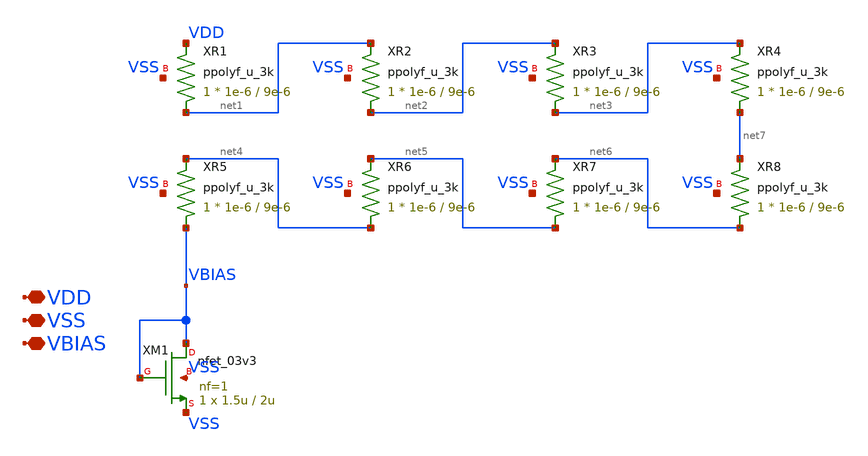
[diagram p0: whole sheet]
** sch_path: designs/libs/core_current-mirror/nbias-gen/nbias-gen.sch
**.subckt nbias-gen VDD VSS VBIAS
*.iopin VDD
*.iopin VSS
*.iopin VBIAS
XM1 VBIAS VBIAS VSS VSS nfet_03v3 L=2u W=1.5u nf=1 ad='int((nf+1)/2) * W/nf * 0.18u' as='int((nf+2)/2) * W/nf * 0.18u'
+ pd='2*int((nf+1)/2) * (W/nf + 0.18u)' ps='2*int((nf+2)/2) * (W/nf + 0.18u)' nrd='0.18u / W' nrs='0.18u / W'
+ sa=0 sb=0 sd=0 m=1
XR1 net1 VDD VSS ppolyf_u_3k r_width=1e-6 r_length=9e-6 m=1
XR2 net2 net1 VSS ppolyf_u_3k r_width=1e-6 r_length=9e-6 m=1
XR3 net3 net2 VSS ppolyf_u_3k r_width=1e-6 r_length=9e-6 m=1
XR4 net7 net3 VSS ppolyf_u_3k r_width=1e-6 r_length=9e-6 m=1
XR5 VBIAS net4 VSS ppolyf_u_3k r_width=1e-6 r_length=9e-6 m=1
XR6 net4 net5 VSS ppolyf_u_3k r_width=1e-6 r_length=9e-6 m=1
XR7 net5 net6 VSS ppolyf_u_3k r_width=1e-6 r_length=9e-6 m=1
XR8 net6 net7 VSS ppolyf_u_3k r_width=1e-6 r_length=9e-6 m=1
**.ends
.end
